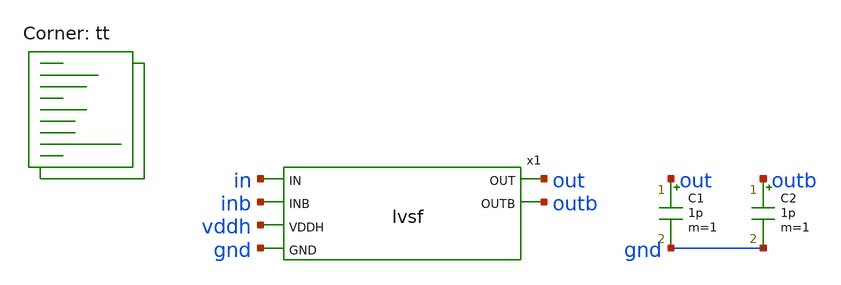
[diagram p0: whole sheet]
** sch_path: xschem/lvsf-tb.sch
**.subckt lvsf-tb
x1 in inb out outb vddh gnd lvsf
C1 out gnd 1p m=1
C2 outb gnd 1p m=1
**** begin user architecture code



  .param max_freq=100e3 period={1/max_freq} time_high={period/2}
  .param delay_vin1={time_high} delay_vin2={time_high*1.5}
  .param lval=100u

  .option wnflag=1
  .option safecurrents

  Vddh vddh gnd dc 5
  Vin  in  gnd pulse(0 1.8 {delay_vin1} 1p 1p {time_high} {period})
  Vinb inb gnd pulse(1.8 0 {delay_vin1} 1p 1p {time_high} {period})

  .control
     reset
     save all
     tran 1n 100u
     write lvsf-tb.raw
     set appendwrite

     *reset
     *save all
     *dc vref 0 1.8 0.1
     *write lvsf-tb.raw
*    quit 0
  .endc



.lib $::SKYWATER_MODELS/sky130.lib.spice tt
**** end user architecture code
**.ends

* expanding   symbol:  lvsf.sym # of pins=6
** sym_path: xschem/lvsf.sym
** sch_path: xschem/lvsf.sch
.subckt lvsf IN INB OUT OUTB VDDH GND
*.ipin IN
*.ipin INB
*.opin OUT
*.opin OUTB
*.ipin VDDH
*.ipin GND
XM2 net4 INB VDDH VDDH sky130_fd_pr__pfet_g5v0d10v5 L=0.5 W=0.42 nf=1 ad='int((nf+1)/2) * W/nf * 0.29'
+ as='int((nf+2)/2) * W/nf * 0.29' pd='2*int((nf+1)/2) * (W/nf + 0.29)' ps='2*int((nf+2)/2) * (W/nf + 0.29)'
+ nrd='0.29 / W' nrs='0.29 / W' sa=0 sb=0 sd=0 mult=1 m=1
XM3 net1 IN VDDH VDDH sky130_fd_pr__pfet_g5v0d10v5 L=0.5 W=0.42 nf=1 ad='int((nf+1)/2) * W/nf * 0.29'
+ as='int((nf+2)/2) * W/nf * 0.29' pd='2*int((nf+1)/2) * (W/nf + 0.29)' ps='2*int((nf+2)/2) * (W/nf + 0.29)'
+ nrd='0.29 / W' nrs='0.29 / W' sa=0 sb=0 sd=0 mult=1 m=1
XM4 net3 net2 net5 VDDH sky130_fd_pr__pfet_g5v0d10v5 L=0.5 W=0.42 nf=1 ad='int((nf+1)/2) * W/nf * 0.29'
+ as='int((nf+2)/2) * W/nf * 0.29' pd='2*int((nf+1)/2) * (W/nf + 0.29)' ps='2*int((nf+2)/2) * (W/nf + 0.29)'
+ nrd='0.29 / W' nrs='0.29 / W' sa=0 sb=0 sd=0 mult=1 m=1
XM5 net2 net3 net1 VDDH sky130_fd_pr__pfet_g5v0d10v5 L=0.5 W=0.42 nf=1 ad='int((nf+1)/2) * W/nf * 0.29'
+ as='int((nf+2)/2) * W/nf * 0.29' pd='2*int((nf+1)/2) * (W/nf + 0.29)' ps='2*int((nf+2)/2) * (W/nf + 0.29)'
+ nrd='0.29 / W' nrs='0.29 / W' sa=0 sb=0 sd=0 mult=1 m=1
XM7 OUTB net3 VDDH VDDH sky130_fd_pr__pfet_g5v0d10v5 L=0.5 W=1.26 nf=1 ad='int((nf+1)/2) * W/nf * 0.29'
+ as='int((nf+2)/2) * W/nf * 0.29' pd='2*int((nf+1)/2) * (W/nf + 0.29)' ps='2*int((nf+2)/2) * (W/nf + 0.29)'
+ nrd='0.29 / W' nrs='0.29 / W' sa=0 sb=0 sd=0 mult=1 m=1
XM9 OUT OUTB VDDH VDDH sky130_fd_pr__pfet_g5v0d10v5 L=0.5 W=1.26 nf=1 ad='int((nf+1)/2) * W/nf * 0.29'
+ as='int((nf+2)/2) * W/nf * 0.29' pd='2*int((nf+1)/2) * (W/nf + 0.29)' ps='2*int((nf+2)/2) * (W/nf + 0.29)'
+ nrd='0.29 / W' nrs='0.29 / W' sa=0 sb=0 sd=0 mult=1 m=1
XM10 net2 IN GND GND sky130_fd_pr__nfet_g5v0d10v5 L=0.5 W=1.26 nf=1 ad='int((nf+1)/2) * W/nf * 0.29'
+ as='int((nf+2)/2) * W/nf * 0.29' pd='2*int((nf+1)/2) * (W/nf + 0.29)' ps='2*int((nf+2)/2) * (W/nf + 0.29)'
+ nrd='0.29 / W' nrs='0.29 / W' sa=0 sb=0 sd=0 mult=1 m=1
XM1 net3 INB GND GND sky130_fd_pr__nfet_g5v0d10v5 L=0.5 W=1.26 nf=1 ad='int((nf+1)/2) * W/nf * 0.29'
+ as='int((nf+2)/2) * W/nf * 0.29' pd='2*int((nf+1)/2) * (W/nf + 0.29)' ps='2*int((nf+2)/2) * (W/nf + 0.29)'
+ nrd='0.29 / W' nrs='0.29 / W' sa=0 sb=0 sd=0 mult=1 m=1
XM6 OUTB net3 GND GND sky130_fd_pr__nfet_g5v0d10v5 L=0.5 W=0.42 nf=1 ad='int((nf+1)/2) * W/nf * 0.29'
+ as='int((nf+2)/2) * W/nf * 0.29' pd='2*int((nf+1)/2) * (W/nf + 0.29)' ps='2*int((nf+2)/2) * (W/nf + 0.29)'
+ nrd='0.29 / W' nrs='0.29 / W' sa=0 sb=0 sd=0 mult=1 m=1
XM8 OUT OUTB GND GND sky130_fd_pr__nfet_g5v0d10v5 L=0.5 W=0.42 nf=1 ad='int((nf+1)/2) * W/nf * 0.29'
+ as='int((nf+2)/2) * W/nf * 0.29' pd='2*int((nf+1)/2) * (W/nf + 0.29)' ps='2*int((nf+2)/2) * (W/nf + 0.29)'
+ nrd='0.29 / W' nrs='0.29 / W' sa=0 sb=0 sd=0 mult=1 m=1
Vmeas net4 net5 0
.save i(vmeas)
.ends

.end
